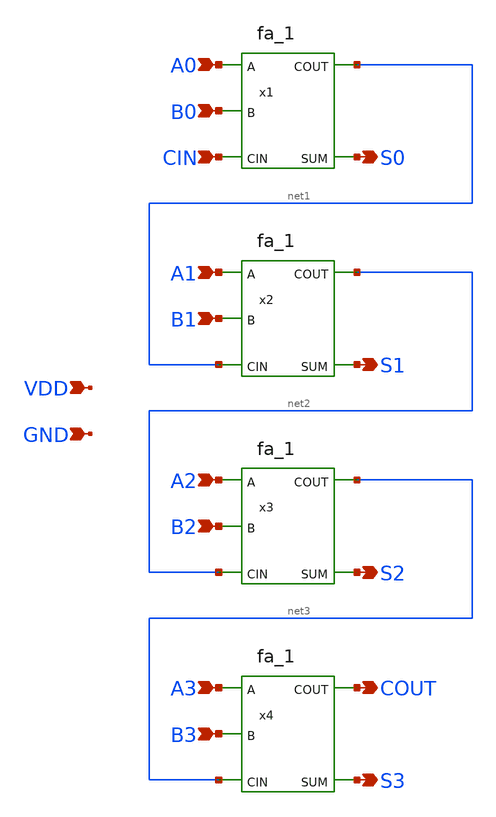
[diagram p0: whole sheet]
** sch_path: xschem/new_adder_4bit.sch
**.subckt new_adder_4bit A0 A1 A2 A3 S0 S1 S2 S3 B0 B1 B2 B3 CIN COUT VDD GND
*.ipin A0
*.ipin A1
*.ipin A2
*.ipin A3
*.opin S0
*.opin S1
*.opin S2
*.opin S3
*.ipin B0
*.ipin B1
*.ipin B2
*.ipin B3
*.ipin CIN
*.opin COUT
*.ipin VDD
*.ipin GND
x1 A0 B0 CIN GND GND VDD VDD net1 S0 sky130_fd_sc_hd__fa_1
x2 A1 B1 net1 GND GND VDD VDD net2 S1 sky130_fd_sc_hd__fa_1
x3 A2 B2 net2 GND GND VDD VDD net3 S2 sky130_fd_sc_hd__fa_1
x4 A3 B3 net3 GND GND VDD VDD COUT S3 sky130_fd_sc_hd__fa_1
**.ends
.end
